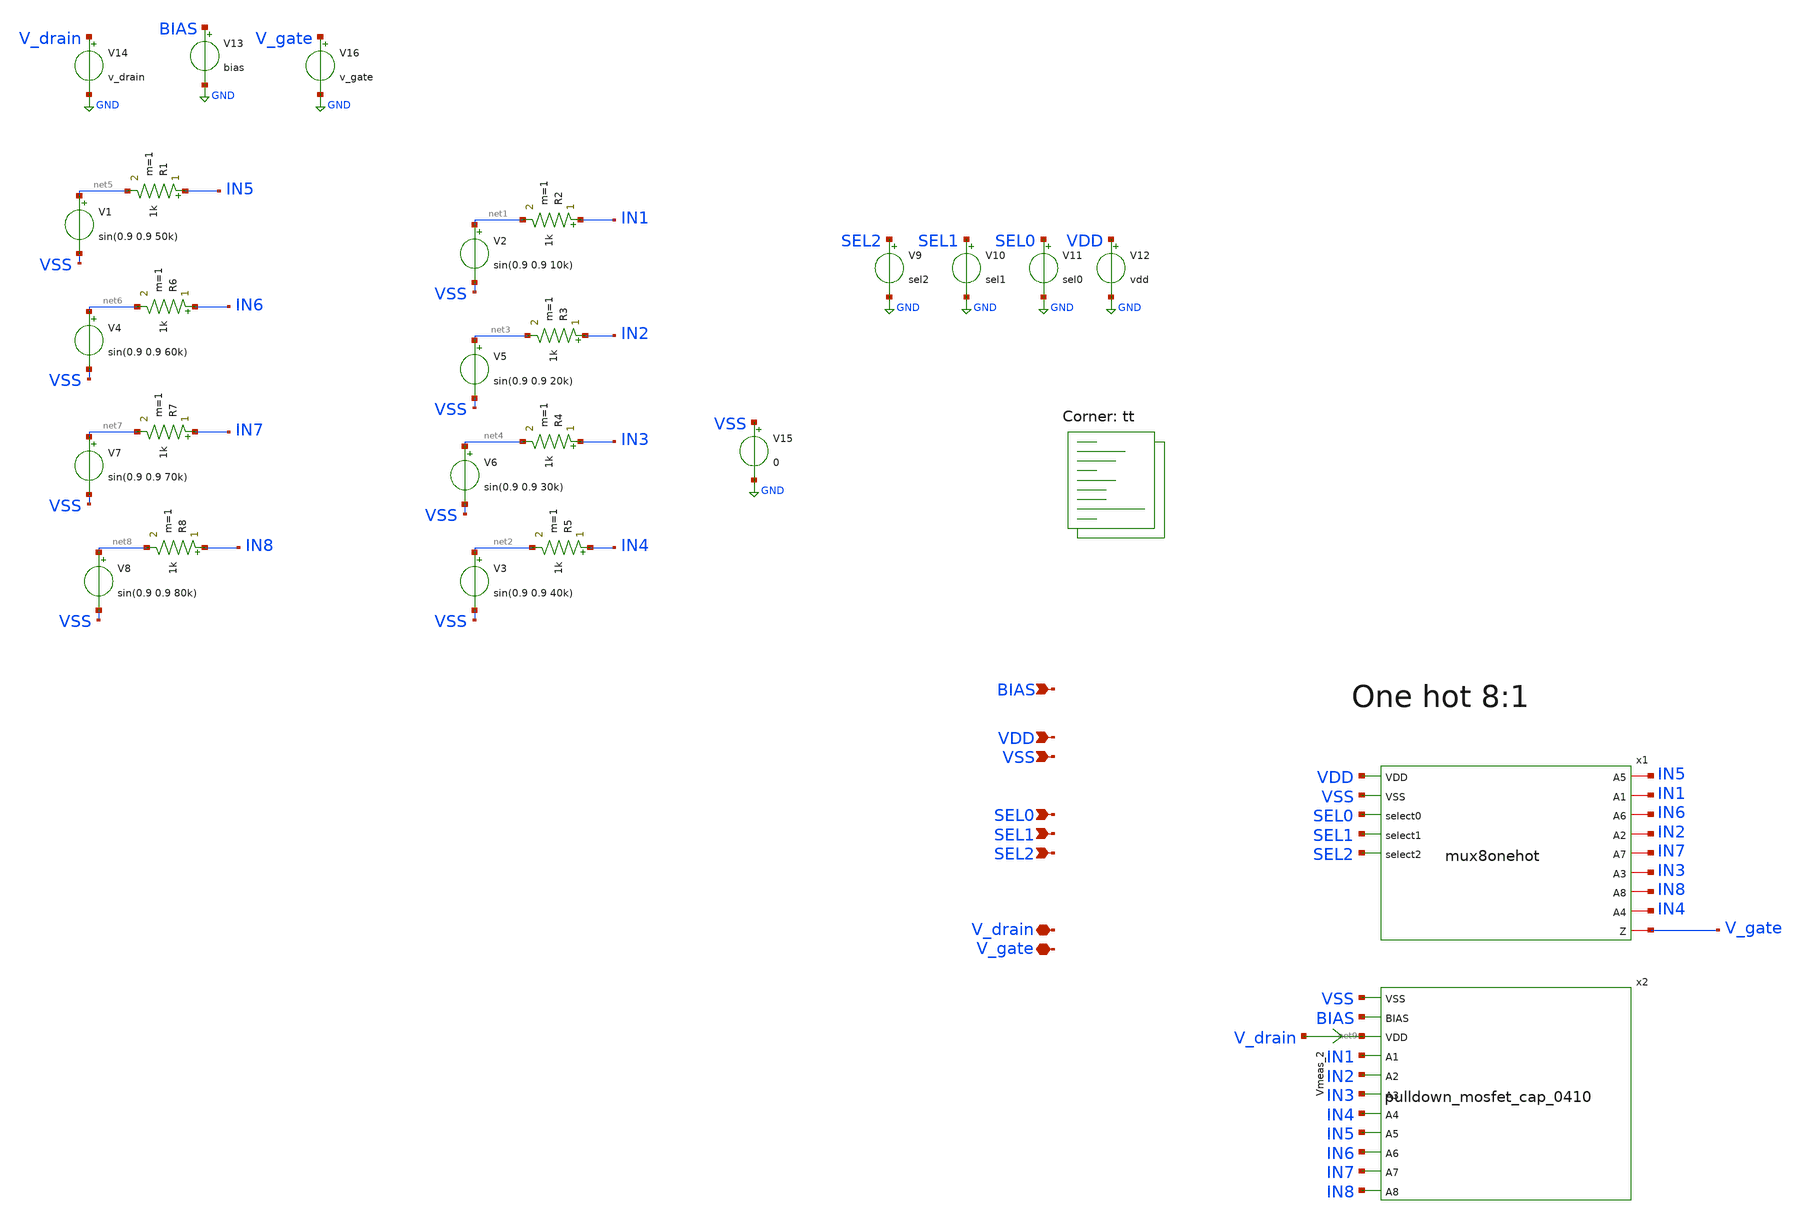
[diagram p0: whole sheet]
** sch_path: sch/tb_mux8onehot_cap_0410.sch
**.subckt tb_mux8onehot_cap_0410 SEL0 SEL1 SEL2 VDD VSS V_gate BIAS V_drain
*.ipin SEL0
*.ipin SEL1
*.ipin SEL2
*.ipin VDD
*.ipin VSS
*.iopin V_gate
*.ipin BIAS
*.iopin V_drain
x1 VDD VSS SEL0 SEL1 IN5 SEL2 IN1 IN6 IN2 IN7 IN3 IN8 IN4 V_gate mux8onehot
x2 VSS BIAS net9 IN1 IN2 IN3 IN4 IN5 IN6 IN7 IN8 pulldown_mosfet_cap_0410
V9 SEL2 GND sel2
V10 SEL1 GND sel1
V11 SEL0 GND sel0
V12 VDD GND vdd
V15 VSS GND 0
V2 net1 VSS sin(0.9 0.9 10k)
V3 net2 VSS sin(0.9 0.9 40k)
V5 net3 VSS sin(0.9 0.9 20k)
V6 net4 VSS sin(0.9 0.9 30k)
R2 IN1 net1 1k m=1
R3 IN2 net3 1k m=1
R4 IN3 net4 1k m=1
R5 IN4 net2 1k m=1
V1 net5 VSS sin(0.9 0.9 50k)
R1 IN5 net5 1k m=1
V4 net6 VSS sin(0.9 0.9 60k)
R6 IN6 net6 1k m=1
V7 net7 VSS sin(0.9 0.9 70k)
R7 IN7 net7 1k m=1
V8 net8 VSS sin(0.9 0.9 80k)
R8 IN8 net8 1k m=1
V13 BIAS GND bias
V14 V_drain GND v_drain
V16 V_gate GND v_gate
Vmeas_2 V_drain net9 0
.save i(vmeas_2)
**** begin user architecture code



.include /home/isshu/pdk/ciel/sky130/versions/0fe599b2afb6708d281543108caf8310912f54af/sky130A/libs.ref/sky130_fd_sc_hd/spice/sky130_fd_sc_hd.spice
.param vdd = 1.8
.param SRCRES = 1k
.param sel0 = 1.8
.param sel1 = 1.8
.param sel2 = 1.8

.param bias = 0.8
.param v_gate = 0.8
.param v_drain = 0


.options savecurrents


.control
set filetype=ascii
save all

* V_drainの初期値、ステップ、終了値を設定
let vd_val = 0
let vd_step = 0.2
let vd_stop = 1.8

* ループ処理でトランジェント解析を繰り返す
while vd_val <= vd_stop
    alter v_14 vd_val
    tran 100p 50n
    let vd_val = vd_val + vd_step
end

* 複数回のrun結果がまとめて出力されます
print all >> simulation_log_mux8onehot_cap_0410_Vdrain.txt
wrdata tb_mux8onehot_cap_0410_Vdrain.dat all
write tb_mux8onehot_cap_0410_Vdrain.raw all
.endc



.lib $::SKYWATER_MODELS/sky130.lib.spice tt
**** end user architecture code
**.ends
.GLOBAL GND
.end
